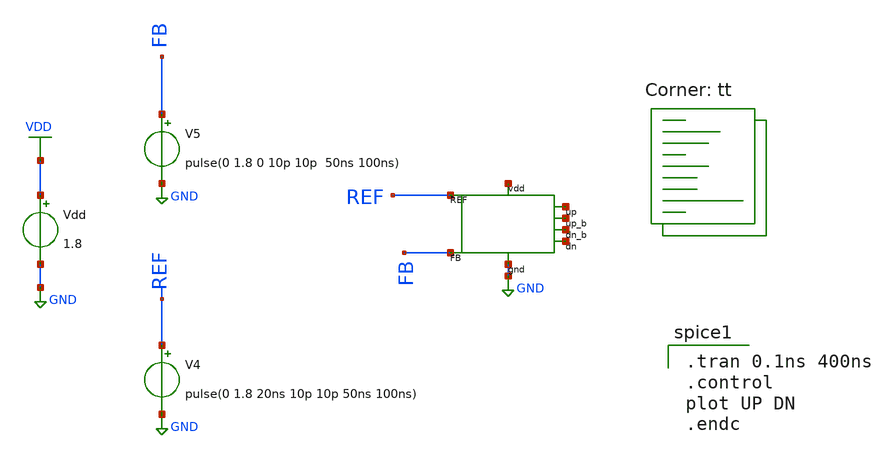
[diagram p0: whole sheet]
** sch_path: pll/pfd_cp_lf_lib/conventional_pfd_tb/xschem/PFD_tb.sch
**.subckt PFD_tb
Vdd VDD GND 1.8
V4 REF GND pulse(0 1.8 20ns 10p 10p 50ns 100ns)
V5 FB GND pulse(0 1.8 0 10p 10p 50ns 100ns)
**** begin user architecture code
.lib $::SKYWATER_MODELS/sky130.lib.spice tt

.tran 0.1ns 400ns
.control
plot UP DN
.endc

**** end user architecture code
**.ends
.GLOBAL GND
.GLOBAL VDD
.end
